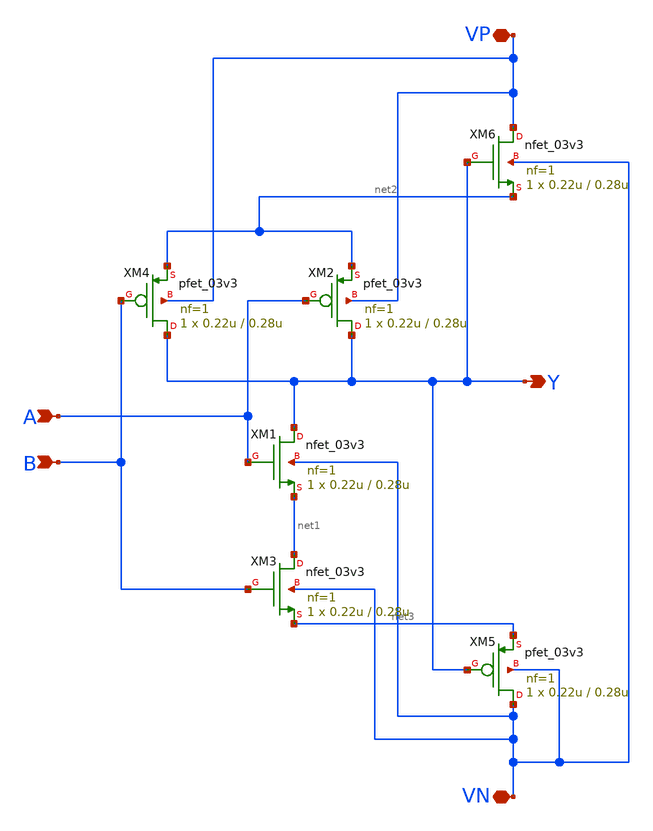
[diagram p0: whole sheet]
** sch_path: dls_nand.sch
**.subckt dls_nand VP A B VN Y
*.iopin VP
*.ipin A
*.ipin B
*.iopin VN
*.opin Y
XM2 Y A net2 VP pfet_03v3 L=0.28u W=0.22u nf=1 ad='int((nf+1)/2) * W/nf * 0.18u' as='int((nf+2)/2) * W/nf * 0.18u'
+ pd='2*int((nf+1)/2) * (W/nf + 0.18u)' ps='2*int((nf+2)/2) * (W/nf + 0.18u)' nrd='0.18u / W' nrs='0.18u / W'
+ sa=0 sb=0 sd=0 m=1 par=1
XM1 Y A net1 VN nfet_03v3 L=0.28u W=0.22u nf=1 ad='int((nf+1)/2) * W/nf * 0.18u' as='int((nf+2)/2) * W/nf * 0.18u'
+ pd='2*int((nf+1)/2) * (W/nf + 0.18u)' ps='2*int((nf+2)/2) * (W/nf + 0.18u)' nrd='0.18u / W' nrs='0.18u / W'
+ sa=0 sb=0 sd=0 m=1 par=1
XM3 net1 B net3 VN nfet_03v3 L=0.28u W=0.22u nf=1 ad='int((nf+1)/2) * W/nf * 0.18u' as='int((nf+2)/2) * W/nf * 0.18u'
+ pd='2*int((nf+1)/2) * (W/nf + 0.18u)' ps='2*int((nf+2)/2) * (W/nf + 0.18u)' nrd='0.18u / W' nrs='0.18u / W'
+ sa=0 sb=0 sd=0 m=1 par=1
XM4 Y B net2 VP pfet_03v3 L=0.28u W=0.22u nf=1 ad='int((nf+1)/2) * W/nf * 0.18u' as='int((nf+2)/2) * W/nf * 0.18u'
+ pd='2*int((nf+1)/2) * (W/nf + 0.18u)' ps='2*int((nf+2)/2) * (W/nf + 0.18u)' nrd='0.18u / W' nrs='0.18u / W'
+ sa=0 sb=0 sd=0 m=1 par=1
XM5 VN Y net3 VN pfet_03v3 L=0.28u W=0.22u nf=1 ad='int((nf+1)/2) * W/nf * 0.18u' as='int((nf+2)/2) * W/nf * 0.18u'
+ pd='2*int((nf+1)/2) * (W/nf + 0.18u)' ps='2*int((nf+2)/2) * (W/nf + 0.18u)' nrd='0.18u / W' nrs='0.18u / W'
+ sa=0 sb=0 sd=0 m=1 par=1
XM6 VP Y net2 VN nfet_03v3 L=0.28u W=0.22u nf=1 ad='int((nf+1)/2) * W/nf * 0.18u' as='int((nf+2)/2) * W/nf * 0.18u'
+ pd='2*int((nf+1)/2) * (W/nf + 0.18u)' ps='2*int((nf+2)/2) * (W/nf + 0.18u)' nrd='0.18u / W' nrs='0.18u / W'
+ sa=0 sb=0 sd=0 m=1 par=1
**.ends
.end
